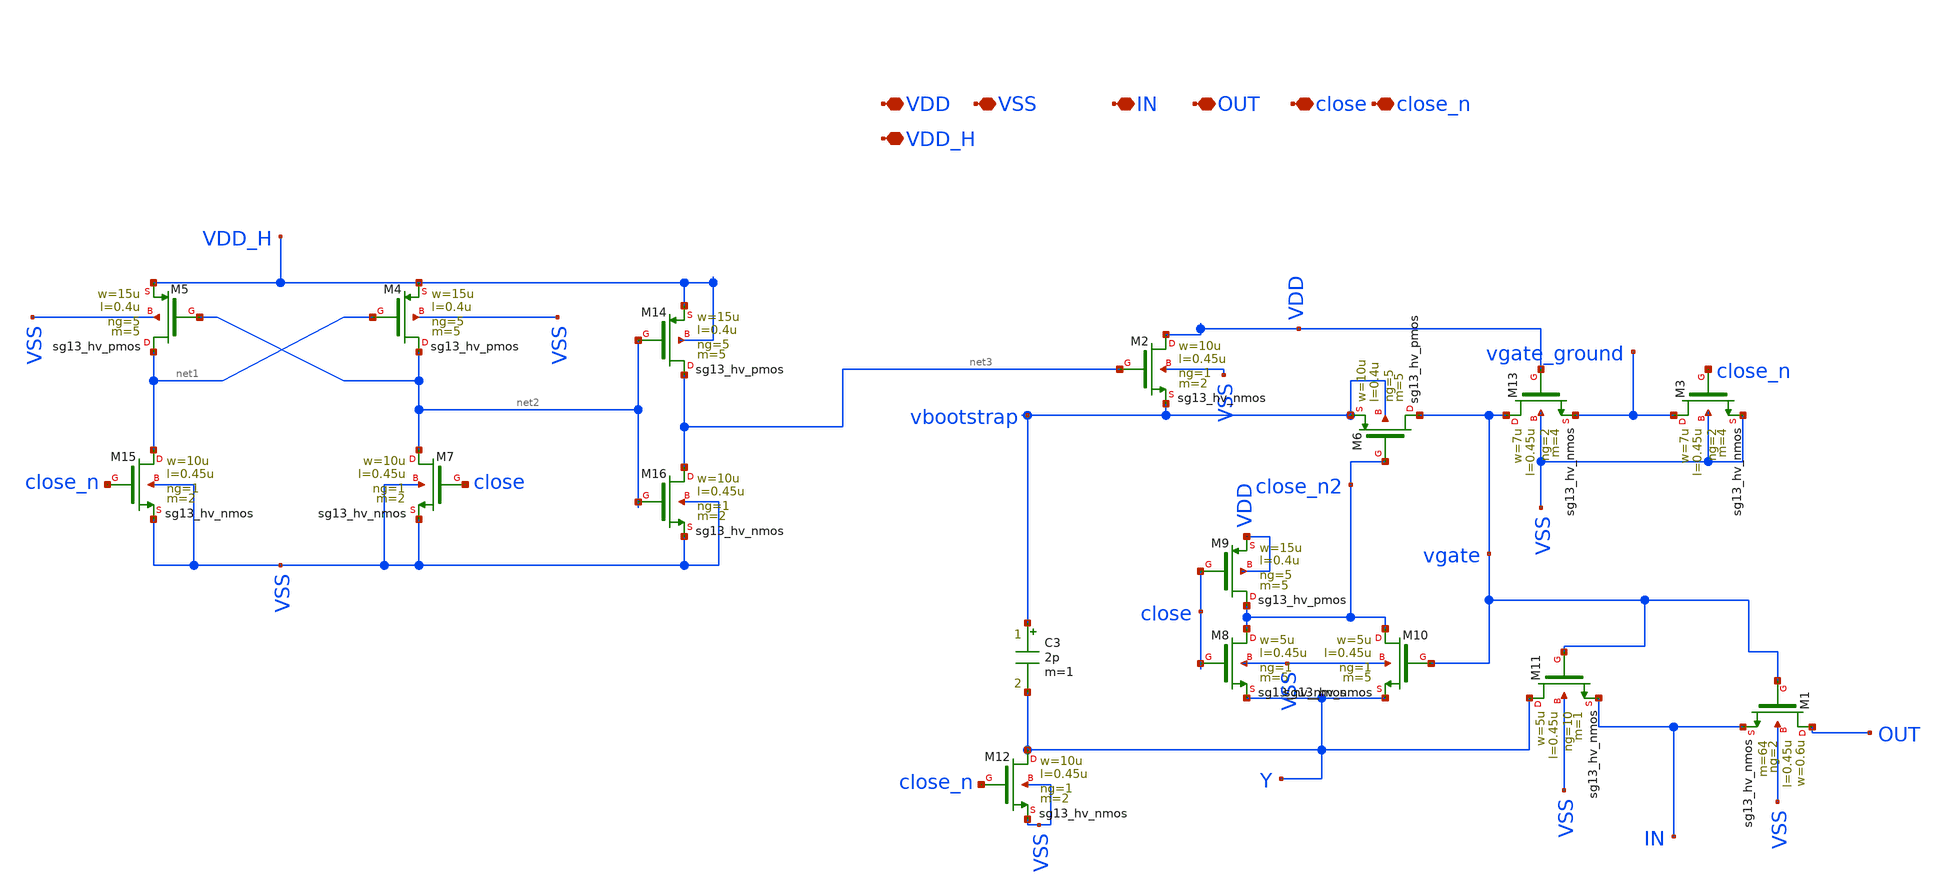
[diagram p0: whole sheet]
** sch_path: xschem/bootstrap/bootstrap.sch
**.subckt bootstrap VDD VSS IN OUT close close_n VDD_H
*.iopin VDD
*.iopin VSS
*.iopin IN
*.iopin OUT
*.iopin close
*.iopin close_n
*.iopin VDD_H
XM6 vgate close_n2 vbootstrap vbootstrap sg13_hv_pmos w=10u l=0.4u ng=5 m=5 mm_ok=1
XM8 close_n2 close Y VSS sg13_hv_nmos w=5u l=0.45u ng=1 m=5 mm_ok=1
XM9 close_n2 close VDD VDD sg13_hv_pmos w=15u l=0.4u ng=5 m=5 mm_ok=1
XM10 close_n2 vgate Y VSS sg13_hv_nmos w=5u l=0.45u ng=1 m=5 mm_ok=1
XM11 Y vgate IN VSS sg13_hv_nmos w=5u l=0.45u ng=10 m=1 mm_ok=1
C3 vbootstrap Y 2p m=1
XM12 Y close_n VSS VSS sg13_hv_nmos w=10u l=0.45u ng=1 m=2 mm_ok=1
XM13 vgate VDD vgate_ground VSS sg13_hv_nmos w=7u l=0.45u ng=2 m=4 mm_ok=1
XM3 vgate_ground close_n VSS VSS sg13_hv_nmos w=7u l=0.45u ng=2 m=4 mm_ok=1
XM1 OUT vgate IN VSS sg13_hv_nmos w=0.6u l=0.45u ng=2 m=64 mm_ok=1
XM2 VDD net3 vbootstrap VSS sg13_hv_nmos w=10u l=0.45u ng=1 m=2 mm_ok=1
XM15 net1 close_n VSS VSS sg13_hv_nmos w=10u l=0.45u ng=1 m=2 mm_ok=1
XM7 net2 close VSS VSS sg13_hv_nmos w=10u l=0.45u ng=1 m=2 mm_ok=1
XM4 net2 net1 VDD_H VSS sg13_hv_pmos w=15u l=0.4u ng=5 m=5 mm_ok=1
XM5 net1 net2 VDD_H VSS sg13_hv_pmos w=15u l=0.4u ng=5 m=5 mm_ok=1
XM14 net3 net2 VDD_H VDD_H sg13_hv_pmos w=15u l=0.4u ng=5 m=5 mm_ok=1
XM16 net3 net2 VSS VSS sg13_hv_nmos w=10u l=0.45u ng=1 m=2 mm_ok=1
**.ends
.end
